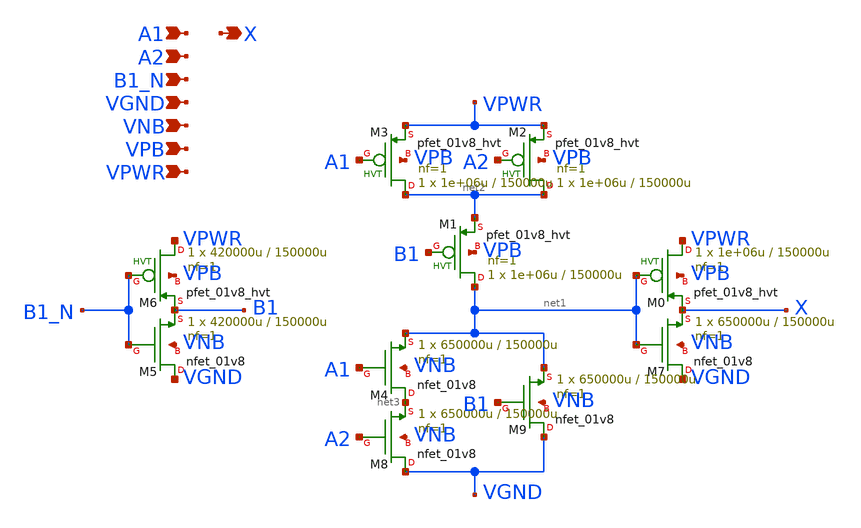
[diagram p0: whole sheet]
** sch_path: schematics/a21bo/sky130_fd_sc_hd__a21bo_1.sch
**.subckt sky130_fd_sc_hd__a21bo_1 A1 A2 B1_N VGND VNB VPB VPWR X
*.ipin A1
*.ipin A2
*.ipin B1_N
*.ipin VGND
*.ipin VNB
*.ipin VPB
*.ipin VPWR
*.opin X
XM7 VGND net1 X VNB sky130_fd_pr__nfet_01v8 L=150000u W=650000u nf=1 ad='int((1 + 1)/2) * 650000u / 1 * 0.29'
+ as='int((1 + 2)/2) * 650000u / 1 * 0.29' pd='2*int((1 + 1)/2) * (650000u / 1 + 0.29)' ps='2*int((1 + 2)/2) * (650000u / 1 + 0.29)'
+ nrd='0.29 / 650000u ' nrs='0.29 / 650000u ' sa=0 sb=0 sd=0 mult=1 m=1
XM2 net2 A2 VPWR VPB sky130_fd_pr__pfet_01v8_hvt L=150000u W=1e+06u nf=1 ad='int((1 + 1)/2) * 1e+06u / 1 * 0.29'
+ as='int((1 + 2)/2) * 1e+06u / 1 * 0.29' pd='2*int((1 + 1)/2) * (1e+06u / 1 + 0.29)' ps='2*int((1 + 2)/2) * (1e+06u / 1 + 0.29)'
+ nrd='0.29 / 1e+06u ' nrs='0.29 / 1e+06u ' sa=0 sb=0 sd=0 mult=1 m=1
XM4 net3 A1 net1 VNB sky130_fd_pr__nfet_01v8 L=150000u W=650000u nf=1 ad='int((1 + 1)/2) * 650000u / 1 * 0.29'
+ as='int((1 + 2)/2) * 650000u / 1 * 0.29' pd='2*int((1 + 1)/2) * (650000u / 1 + 0.29)' ps='2*int((1 + 2)/2) * (650000u / 1 + 0.29)'
+ nrd='0.29 / 650000u ' nrs='0.29 / 650000u ' sa=0 sb=0 sd=0 mult=1 m=1
XM0 VPWR net1 X VPB sky130_fd_pr__pfet_01v8_hvt L=150000u W=1e+06u nf=1 ad='int((1 + 1)/2) * 1e+06u / 1 * 0.29'
+ as='int((1 + 2)/2) * 1e+06u / 1 * 0.29' pd='2*int((1 + 1)/2) * (1e+06u / 1 + 0.29)' ps='2*int((1 + 2)/2) * (1e+06u / 1 + 0.29)'
+ nrd='0.29 / 1e+06u ' nrs='0.29 / 1e+06u ' sa=0 sb=0 sd=0 mult=1 m=1
XM3 net2 A1 VPWR VPB sky130_fd_pr__pfet_01v8_hvt L=150000u W=1e+06u nf=1 ad='int((1 + 1)/2) * 1e+06u / 1 * 0.29'
+ as='int((1 + 2)/2) * 1e+06u / 1 * 0.29' pd='2*int((1 + 1)/2) * (1e+06u / 1 + 0.29)' ps='2*int((1 + 2)/2) * (1e+06u / 1 + 0.29)'
+ nrd='0.29 / 1e+06u ' nrs='0.29 / 1e+06u ' sa=0 sb=0 sd=0 mult=1 m=1
XM1 net1 B1 net2 VPB sky130_fd_pr__pfet_01v8_hvt L=150000u W=1e+06u nf=1 ad='int((1 + 1)/2) * 1e+06u / 1 * 0.29'
+ as='int((1 + 2)/2) * 1e+06u / 1 * 0.29' pd='2*int((1 + 1)/2) * (1e+06u / 1 + 0.29)' ps='2*int((1 + 2)/2) * (1e+06u / 1 + 0.29)'
+ nrd='0.29 / 1e+06u ' nrs='0.29 / 1e+06u ' sa=0 sb=0 sd=0 mult=1 m=1
XM8 VGND A2 net3 VNB sky130_fd_pr__nfet_01v8 L=150000u W=650000u nf=1 ad='int((1 + 1)/2) * 650000u / 1 * 0.29'
+ as='int((1 + 2)/2) * 650000u / 1 * 0.29' pd='2*int((1 + 1)/2) * (650000u / 1 + 0.29)' ps='2*int((1 + 2)/2) * (650000u / 1 + 0.29)'
+ nrd='0.29 / 650000u ' nrs='0.29 / 650000u ' sa=0 sb=0 sd=0 mult=1 m=1
XM5 VGND B1_N B1 VNB sky130_fd_pr__nfet_01v8 L=150000u W=420000u nf=1 ad='int((1 + 1)/2) * 420000u / 1 * 0.29'
+ as='int((1 + 2)/2) * 420000u / 1 * 0.29' pd='2*int((1 + 1)/2) * (420000u / 1 + 0.29)' ps='2*int((1 + 2)/2) * (420000u / 1 + 0.29)'
+ nrd='0.29 / 420000u ' nrs='0.29 / 420000u ' sa=0 sb=0 sd=0 mult=1 m=1
XM6 VPWR B1_N B1 VPB sky130_fd_pr__pfet_01v8_hvt L=150000u W=420000u nf=1 ad='int((1 + 1)/2) * 420000u / 1 * 0.29'
+ as='int((1 + 2)/2) * 420000u / 1 * 0.29' pd='2*int((1 + 1)/2) * (420000u / 1 + 0.29)' ps='2*int((1 + 2)/2) * (420000u / 1 + 0.29)'
+ nrd='0.29 / 420000u ' nrs='0.29 / 420000u ' sa=0 sb=0 sd=0 mult=1 m=1
XM9 VGND B1 net1 VNB sky130_fd_pr__nfet_01v8 L=150000u W=650000u nf=1 ad='int((1 + 1)/2) * 650000u / 1 * 0.29'
+ as='int((1 + 2)/2) * 650000u / 1 * 0.29' pd='2*int((1 + 1)/2) * (650000u / 1 + 0.29)' ps='2*int((1 + 2)/2) * (650000u / 1 + 0.29)'
+ nrd='0.29 / 650000u ' nrs='0.29 / 650000u ' sa=0 sb=0 sd=0 mult=1 m=1
**.ends
.end
